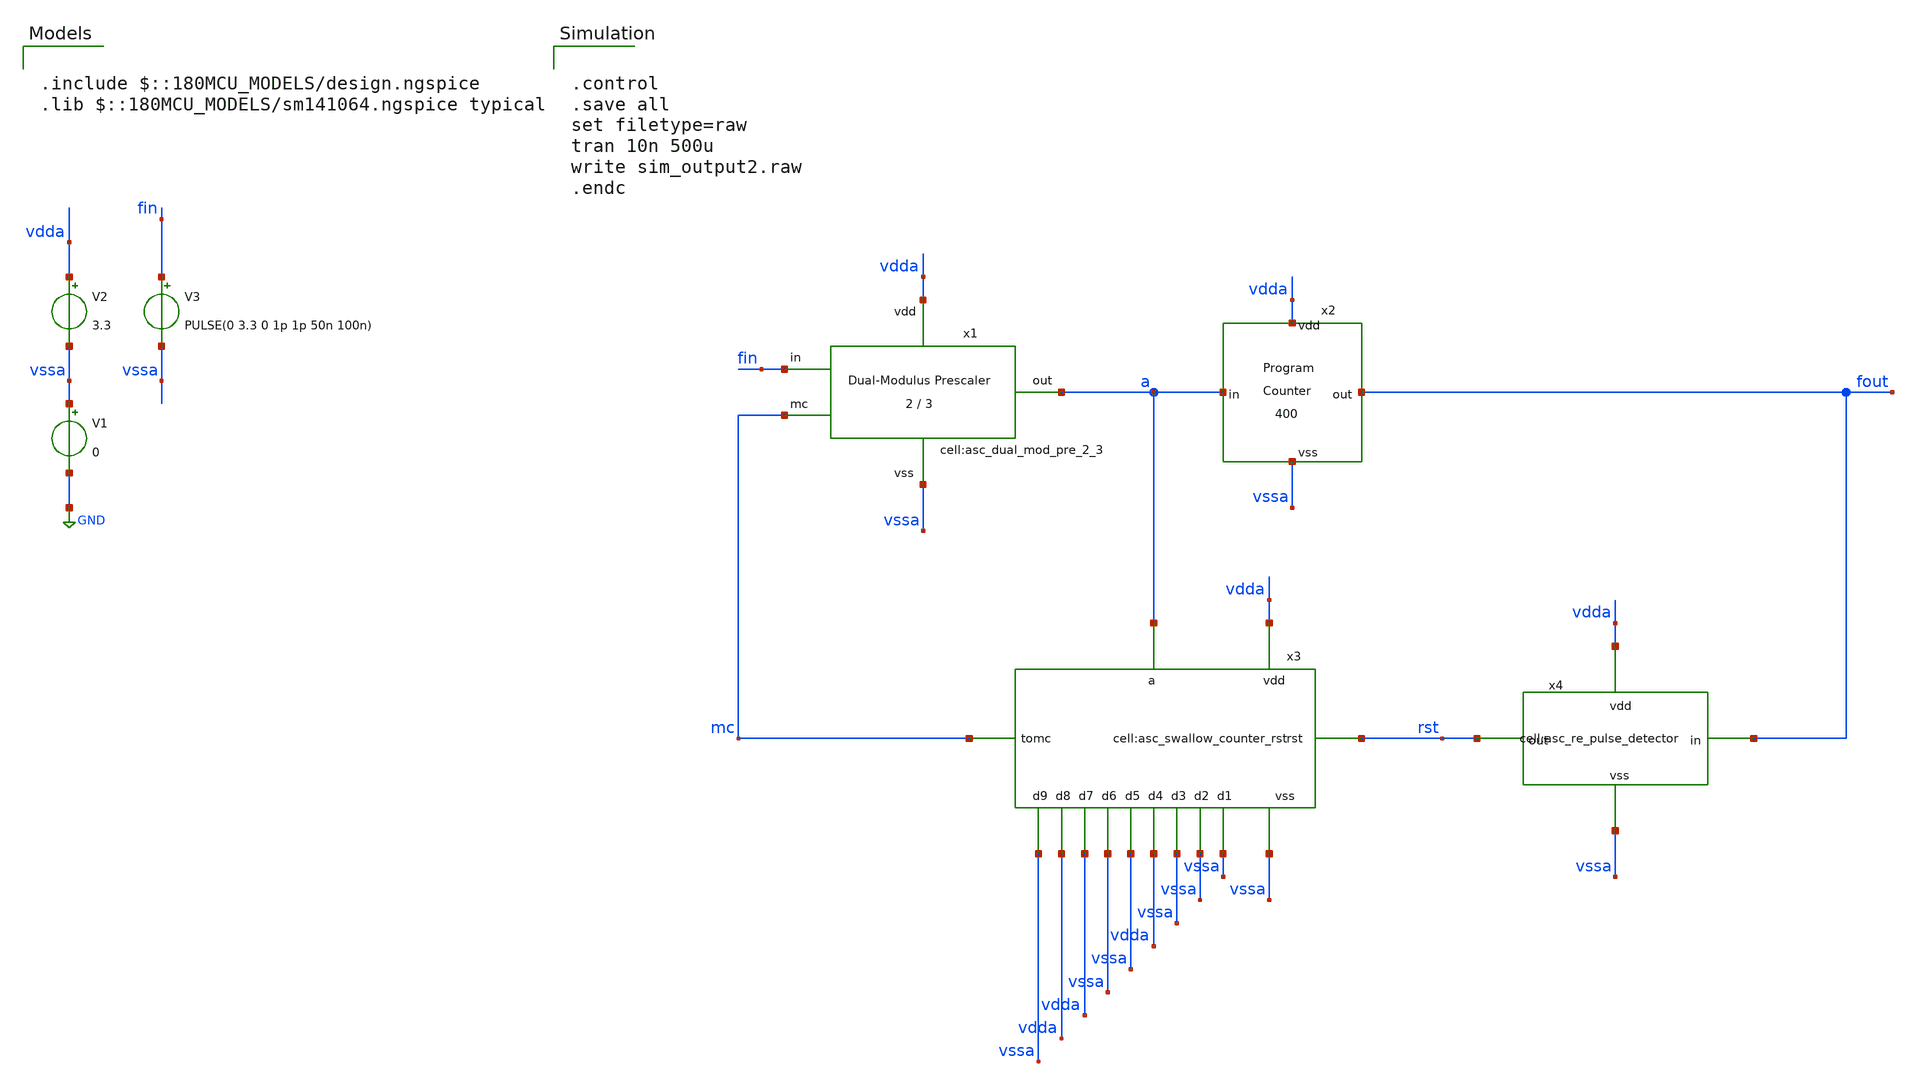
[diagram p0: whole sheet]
** sch_path: designs/libs/tb_analog/tb_pulse_swallow_divider/tb_pulse_swallow_divider.sch
**.subckt tb_pulse_swallow_divider
V1 vssa GND 0
V2 vdda vssa 3.3
V3 fin vssa PULSE(0 3.3 0 1p 1p 50n 100n)
x1 vdda vssa a fin mc asc_dual_mod_pre_2_3
x2 a fout vdda vssa asc_program_counter_400
x4 vdda rst vssa fout asc_re_pulse_detector
x3 mc vssa vdda vdda vssa vssa vdda vssa vssa vssa vssa rst vdda a asc_swallow_counter_rst
**** begin user architecture code

.include $::180MCU_MODELS/design.ngspice
.lib $::180MCU_MODELS/sm141064.ngspice typical



.control
.save all
set filetype=raw
tran 10n 500u
write sim_output2.raw
.endc


**** end user architecture code
**.ends
.GLOBAL GND
.end
